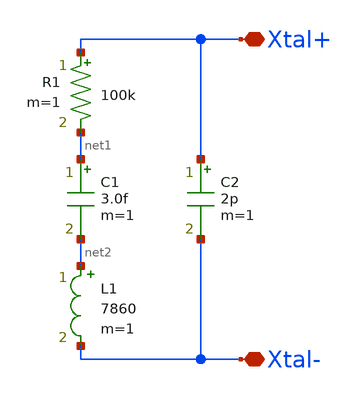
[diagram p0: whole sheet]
** sch_path: design/THESIS_EXP_RO_INVERTER_SKY130A/hard_xtal.sch
**.subckt hard_xtal Xtal+ Xtal-
*.iopin Xtal+
*.iopin Xtal-
R1 Xtal+ net1 100k m=1
C1 net1 net2 3.0f m=1
L1 net2 Xtal- 7860 m=1
C2 Xtal+ Xtal- 2p m=1
**.ends
.end
